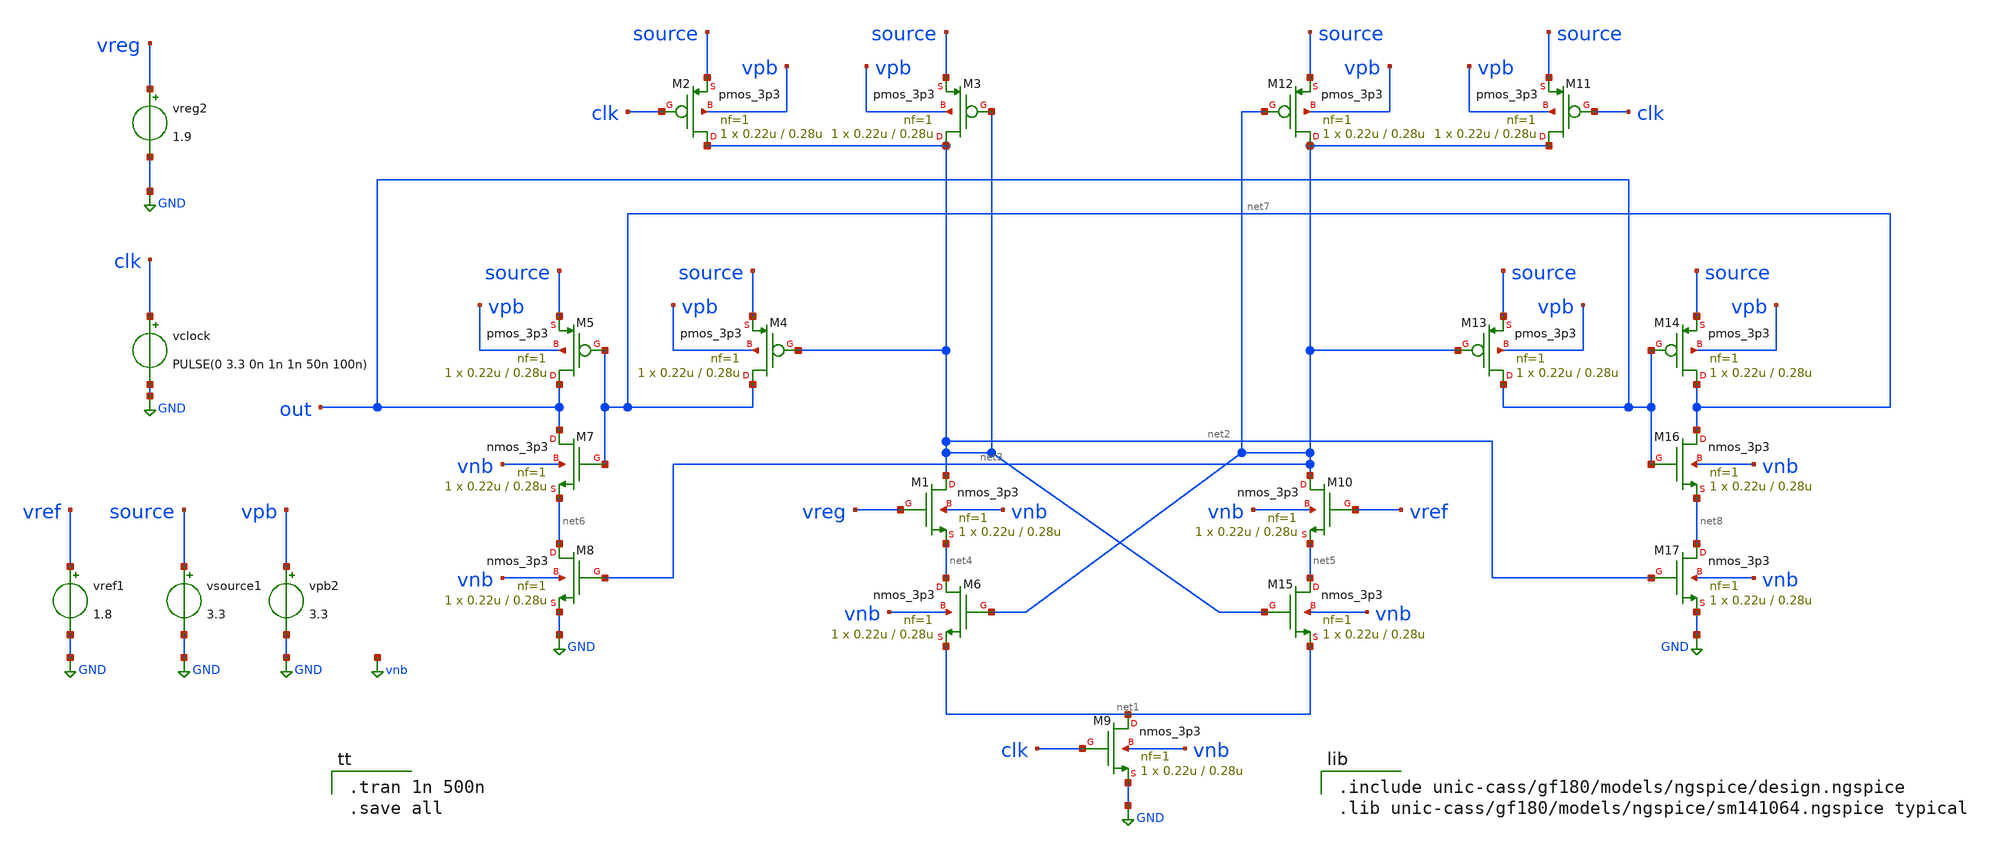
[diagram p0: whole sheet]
** sch_path: datdt/comaparator_latch.sch
**.subckt comaparator_latch
XM1 net2 vreg net4 vnb nmos_3p3 L=0.28u W=0.22u nf=1 ad='int((nf+1)/2) * W/nf * 0.18u' as='int((nf+2)/2) * W/nf * 0.18u'
+ pd='2*int((nf+1)/2) * (W/nf + 0.18u)' ps='2*int((nf+2)/2) * (W/nf + 0.18u)' nrd='0.18u / W' nrs='0.18u / W'
+ sa=0 sb=0 sd=0 m=1
XM2 net2 clk source vpb pmos_3p3 L=0.28u W=0.22u nf=1 ad='int((nf+1)/2) * W/nf * 0.18u' as='int((nf+2)/2) * W/nf * 0.18u'
+ pd='2*int((nf+1)/2) * (W/nf + 0.18u)' ps='2*int((nf+2)/2) * (W/nf + 0.18u)' nrd='0.18u / W' nrs='0.18u / W'
+ sa=0 sb=0 sd=0 m=1
XM3 net2 net2 source vpb pmos_3p3 L=0.28u W=0.22u nf=1 ad='int((nf+1)/2) * W/nf * 0.18u' as='int((nf+2)/2) * W/nf * 0.18u'
+ pd='2*int((nf+1)/2) * (W/nf + 0.18u)' ps='2*int((nf+2)/2) * (W/nf + 0.18u)' nrd='0.18u / W' nrs='0.18u / W'
+ sa=0 sb=0 sd=0 m=1
XM4 net7 net2 source vpb pmos_3p3 L=0.28u W=0.22u nf=1 ad='int((nf+1)/2) * W/nf * 0.18u' as='int((nf+2)/2) * W/nf * 0.18u'
+ pd='2*int((nf+1)/2) * (W/nf + 0.18u)' ps='2*int((nf+2)/2) * (W/nf + 0.18u)' nrd='0.18u / W' nrs='0.18u / W'
+ sa=0 sb=0 sd=0 m=1
XM5 out net7 source vpb pmos_3p3 L=0.28u W=0.22u nf=1 ad='int((nf+1)/2) * W/nf * 0.18u' as='int((nf+2)/2) * W/nf * 0.18u'
+ pd='2*int((nf+1)/2) * (W/nf + 0.18u)' ps='2*int((nf+2)/2) * (W/nf + 0.18u)' nrd='0.18u / W' nrs='0.18u / W'
+ sa=0 sb=0 sd=0 m=1
XM6 net4 net3 net1 vnb nmos_3p3 L=0.28u W=0.22u nf=1 ad='int((nf+1)/2) * W/nf * 0.18u' as='int((nf+2)/2) * W/nf * 0.18u'
+ pd='2*int((nf+1)/2) * (W/nf + 0.18u)' ps='2*int((nf+2)/2) * (W/nf + 0.18u)' nrd='0.18u / W' nrs='0.18u / W'
+ sa=0 sb=0 sd=0 m=1
XM7 out net7 net6 vnb nmos_3p3 L=0.28u W=0.22u nf=1 ad='int((nf+1)/2) * W/nf * 0.18u' as='int((nf+2)/2) * W/nf * 0.18u'
+ pd='2*int((nf+1)/2) * (W/nf + 0.18u)' ps='2*int((nf+2)/2) * (W/nf + 0.18u)' nrd='0.18u / W' nrs='0.18u / W'
+ sa=0 sb=0 sd=0 m=1
XM8 net6 net3 GND vnb nmos_3p3 L=0.28u W=0.22u nf=1 ad='int((nf+1)/2) * W/nf * 0.18u' as='int((nf+2)/2) * W/nf * 0.18u'
+ pd='2*int((nf+1)/2) * (W/nf + 0.18u)' ps='2*int((nf+2)/2) * (W/nf + 0.18u)' nrd='0.18u / W' nrs='0.18u / W'
+ sa=0 sb=0 sd=0 m=1
XM9 net1 clk GND vnb nmos_3p3 L=0.28u W=0.22u nf=1 ad='int((nf+1)/2) * W/nf * 0.18u' as='int((nf+2)/2) * W/nf * 0.18u'
+ pd='2*int((nf+1)/2) * (W/nf + 0.18u)' ps='2*int((nf+2)/2) * (W/nf + 0.18u)' nrd='0.18u / W' nrs='0.18u / W'
+ sa=0 sb=0 sd=0 m=1
XM10 net3 vref net5 vnb nmos_3p3 L=0.28u W=0.22u nf=1 ad='int((nf+1)/2) * W/nf * 0.18u' as='int((nf+2)/2) * W/nf * 0.18u'
+ pd='2*int((nf+1)/2) * (W/nf + 0.18u)' ps='2*int((nf+2)/2) * (W/nf + 0.18u)' nrd='0.18u / W' nrs='0.18u / W'
+ sa=0 sb=0 sd=0 m=1
XM11 net3 clk source vpb pmos_3p3 L=0.28u W=0.22u nf=1 ad='int((nf+1)/2) * W/nf * 0.18u' as='int((nf+2)/2) * W/nf * 0.18u'
+ pd='2*int((nf+1)/2) * (W/nf + 0.18u)' ps='2*int((nf+2)/2) * (W/nf + 0.18u)' nrd='0.18u / W' nrs='0.18u / W'
+ sa=0 sb=0 sd=0 m=1
XM12 net3 net3 source vpb pmos_3p3 L=0.28u W=0.22u nf=1 ad='int((nf+1)/2) * W/nf * 0.18u' as='int((nf+2)/2) * W/nf * 0.18u'
+ pd='2*int((nf+1)/2) * (W/nf + 0.18u)' ps='2*int((nf+2)/2) * (W/nf + 0.18u)' nrd='0.18u / W' nrs='0.18u / W'
+ sa=0 sb=0 sd=0 m=1
XM13 out net3 source vpb pmos_3p3 L=0.28u W=0.22u nf=1 ad='int((nf+1)/2) * W/nf * 0.18u' as='int((nf+2)/2) * W/nf * 0.18u'
+ pd='2*int((nf+1)/2) * (W/nf + 0.18u)' ps='2*int((nf+2)/2) * (W/nf + 0.18u)' nrd='0.18u / W' nrs='0.18u / W'
+ sa=0 sb=0 sd=0 m=1
XM14 net7 out source vpb pmos_3p3 L=0.28u W=0.22u nf=1 ad='int((nf+1)/2) * W/nf * 0.18u' as='int((nf+2)/2) * W/nf * 0.18u'
+ pd='2*int((nf+1)/2) * (W/nf + 0.18u)' ps='2*int((nf+2)/2) * (W/nf + 0.18u)' nrd='0.18u / W' nrs='0.18u / W'
+ sa=0 sb=0 sd=0 m=1
XM15 net5 net2 net1 vnb nmos_3p3 L=0.28u W=0.22u nf=1 ad='int((nf+1)/2) * W/nf * 0.18u' as='int((nf+2)/2) * W/nf * 0.18u'
+ pd='2*int((nf+1)/2) * (W/nf + 0.18u)' ps='2*int((nf+2)/2) * (W/nf + 0.18u)' nrd='0.18u / W' nrs='0.18u / W'
+ sa=0 sb=0 sd=0 m=1
XM16 net7 out net8 vnb nmos_3p3 L=0.28u W=0.22u nf=1 ad='int((nf+1)/2) * W/nf * 0.18u' as='int((nf+2)/2) * W/nf * 0.18u'
+ pd='2*int((nf+1)/2) * (W/nf + 0.18u)' ps='2*int((nf+2)/2) * (W/nf + 0.18u)' nrd='0.18u / W' nrs='0.18u / W'
+ sa=0 sb=0 sd=0 m=1
XM17 net8 net2 GND vnb nmos_3p3 L=0.28u W=0.22u nf=1 ad='int((nf+1)/2) * W/nf * 0.18u' as='int((nf+2)/2) * W/nf * 0.18u'
+ pd='2*int((nf+1)/2) * (W/nf + 0.18u)' ps='2*int((nf+2)/2) * (W/nf + 0.18u)' nrd='0.18u / W' nrs='0.18u / W'
+ sa=0 sb=0 sd=0 m=1
vclock clk GND PULSE(0 3.3 0n 1n 1n 50n 100n)
vref1 vref GND 1.8
vsource1 source GND 3.3
vpb2 vpb GND 3.3
vreg2 vreg GND 1.9
**** begin user architecture code

.include unic-cass/gf180/models/ngspice/design.ngspice
.lib unic-cass/gf180/models/ngspice/sm141064.ngspice typical


.tran 1n 500n
.save all

**** end user architecture code
**.ends
.GLOBAL GND
.GLOBAL vnb
.end
